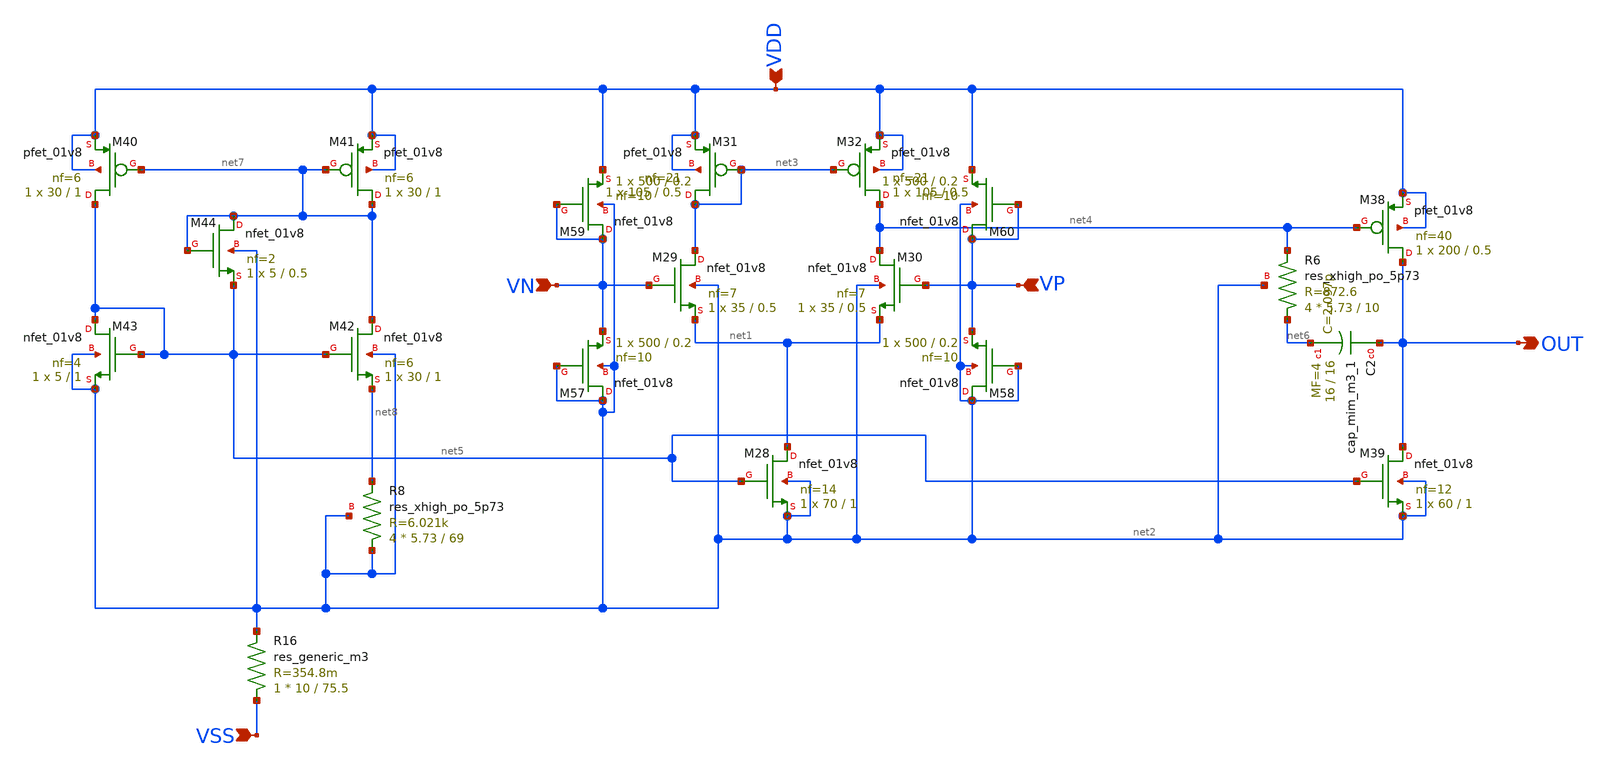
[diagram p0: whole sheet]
** sch_path: DeltaSigma/xschem/C2S2_Amp_F_I.sch
**.subckt C2S2_Amp_F_I VN VDD VSS VP OUT
*.ipin VN
*.ipin VDD
*.ipin VSS
*.ipin VP
*.opin OUT
XM28 net1 net5 net2 net2 sky130_fd_pr__nfet_01v8 L=1 W=70 nf=14 ad='int((nf+1)/2) * W/nf * 0.29' as='int((nf+2)/2) * W/nf * 0.29'
+ pd='2*int((nf+1)/2) * (W/nf + 0.29)' ps='2*int((nf+2)/2) * (W/nf + 0.29)' nrd='0.29 / W' nrs='0.29 / W'
+ sa=0 sb=0 sd=0 mult=1 m=1
XM29 net3 VN net1 net2 sky130_fd_pr__nfet_01v8 L=0.5 W=35 nf=7 ad='int((nf+1)/2) * W/nf * 0.29' as='int((nf+2)/2) * W/nf * 0.29'
+ pd='2*int((nf+1)/2) * (W/nf + 0.29)' ps='2*int((nf+2)/2) * (W/nf + 0.29)' nrd='0.29 / W' nrs='0.29 / W'
+ sa=0 sb=0 sd=0 mult=1 m=1
XM30 net4 VP net1 net2 sky130_fd_pr__nfet_01v8 L=0.5 W=35 nf=7 ad='int((nf+1)/2) * W/nf * 0.29' as='int((nf+2)/2) * W/nf * 0.29'
+ pd='2*int((nf+1)/2) * (W/nf + 0.29)' ps='2*int((nf+2)/2) * (W/nf + 0.29)' nrd='0.29 / W' nrs='0.29 / W'
+ sa=0 sb=0 sd=0 mult=1 m=1
XM31 net3 net3 VDD VDD sky130_fd_pr__pfet_01v8 L=0.5 W=105 nf=21 ad='int((nf+1)/2) * W/nf * 0.29' as='int((nf+2)/2) * W/nf * 0.29'
+ pd='2*int((nf+1)/2) * (W/nf + 0.29)' ps='2*int((nf+2)/2) * (W/nf + 0.29)' nrd='0.29 / W' nrs='0.29 / W'
+ sa=0 sb=0 sd=0 mult=1 m=1
XM32 net4 net3 VDD VDD sky130_fd_pr__pfet_01v8 L=0.5 W=105 nf=21 ad='int((nf+1)/2) * W/nf * 0.29' as='int((nf+2)/2) * W/nf * 0.29'
+ pd='2*int((nf+1)/2) * (W/nf + 0.29)' ps='2*int((nf+2)/2) * (W/nf + 0.29)' nrd='0.29 / W' nrs='0.29 / W'
+ sa=0 sb=0 sd=0 mult=1 m=1
XM38 OUT net4 VDD VDD sky130_fd_pr__pfet_01v8 L=0.5 W=200 nf=40 ad='int((nf+1)/2) * W/nf * 0.29' as='int((nf+2)/2) * W/nf * 0.29'
+ pd='2*int((nf+1)/2) * (W/nf + 0.29)' ps='2*int((nf+2)/2) * (W/nf + 0.29)' nrd='0.29 / W' nrs='0.29 / W'
+ sa=0 sb=0 sd=0 mult=1 m=1
XM39 OUT net5 net2 net2 sky130_fd_pr__nfet_01v8 L=1 W=60 nf=12 ad='int((nf+1)/2) * W/nf * 0.29' as='int((nf+2)/2) * W/nf * 0.29'
+ pd='2*int((nf+1)/2) * (W/nf + 0.29)' ps='2*int((nf+2)/2) * (W/nf + 0.29)' nrd='0.29 / W' nrs='0.29 / W'
+ sa=0 sb=0 sd=0 mult=1 m=1
XC2 OUT net6 sky130_fd_pr__cap_mim_m3_1 W=16 L=16 MF=4 m=4
XR6 net6 net4 net2 sky130_fd_pr__res_xhigh_po_5p73 L=10 mult=4 m=4
XM40 net5 net7 VDD VDD sky130_fd_pr__pfet_01v8 L=1 W=30 nf=6 ad='int((nf+1)/2) * W/nf * 0.29' as='int((nf+2)/2) * W/nf * 0.29'
+ pd='2*int((nf+1)/2) * (W/nf + 0.29)' ps='2*int((nf+2)/2) * (W/nf + 0.29)' nrd='0.29 / W' nrs='0.29 / W'
+ sa=0 sb=0 sd=0 mult=1 m=1
XM41 net7 net7 VDD VDD sky130_fd_pr__pfet_01v8 L=1 W=30 nf=6 ad='int((nf+1)/2) * W/nf * 0.29' as='int((nf+2)/2) * W/nf * 0.29'
+ pd='2*int((nf+1)/2) * (W/nf + 0.29)' ps='2*int((nf+2)/2) * (W/nf + 0.29)' nrd='0.29 / W' nrs='0.29 / W'
+ sa=0 sb=0 sd=0 mult=1 m=1
XM42 net7 net5 net8 net2 sky130_fd_pr__nfet_01v8 L=1 W=30 nf=6 ad='int((nf+1)/2) * W/nf * 0.29' as='int((nf+2)/2) * W/nf * 0.29'
+ pd='2*int((nf+1)/2) * (W/nf + 0.29)' ps='2*int((nf+2)/2) * (W/nf + 0.29)' nrd='0.29 / W' nrs='0.29 / W'
+ sa=0 sb=0 sd=0 mult=1 m=1
XM43 net5 net5 net2 net2 sky130_fd_pr__nfet_01v8 L=1 W=5 nf=4 ad='int((nf+1)/2) * W/nf * 0.29' as='int((nf+2)/2) * W/nf * 0.29'
+ pd='2*int((nf+1)/2) * (W/nf + 0.29)' ps='2*int((nf+2)/2) * (W/nf + 0.29)' nrd='0.29 / W' nrs='0.29 / W'
+ sa=0 sb=0 sd=0 mult=1 m=1
XM44 net7 net7 net5 net2 sky130_fd_pr__nfet_01v8 L=0.5 W=5 nf=2 ad='int((nf+1)/2) * W/nf * 0.29' as='int((nf+2)/2) * W/nf * 0.29'
+ pd='2*int((nf+1)/2) * (W/nf + 0.29)' ps='2*int((nf+2)/2) * (W/nf + 0.29)' nrd='0.29 / W' nrs='0.29 / W'
+ sa=0 sb=0 sd=0 mult=1 m=1
XR8 net2 net8 net2 sky130_fd_pr__res_xhigh_po_5p73 L=69 mult=4 m=4
R16 VSS net2 sky130_fd_pr__res_generic_m3 W=10 L=75.5 m=1
XM57 net2 net2 VN net2 sky130_fd_pr__nfet_01v8 L=0.2 W=500 nf=10 ad='int((nf+1)/2) * W/nf * 0.29' as='int((nf+2)/2) * W/nf * 0.29'
+ pd='2*int((nf+1)/2) * (W/nf + 0.29)' ps='2*int((nf+2)/2) * (W/nf + 0.29)' nrd='0.29 / W' nrs='0.29 / W'
+ sa=0 sb=0 sd=0 mult=1 m=1
XM58 net2 net2 VP net2 sky130_fd_pr__nfet_01v8 L=0.2 W=500 nf=10 ad='int((nf+1)/2) * W/nf * 0.29' as='int((nf+2)/2) * W/nf * 0.29'
+ pd='2*int((nf+1)/2) * (W/nf + 0.29)' ps='2*int((nf+2)/2) * (W/nf + 0.29)' nrd='0.29 / W' nrs='0.29 / W'
+ sa=0 sb=0 sd=0 mult=1 m=1
XM59 VN VN VDD net2 sky130_fd_pr__nfet_01v8 L=0.2 W=500 nf=10 ad='int((nf+1)/2) * W/nf * 0.29' as='int((nf+2)/2) * W/nf * 0.29'
+ pd='2*int((nf+1)/2) * (W/nf + 0.29)' ps='2*int((nf+2)/2) * (W/nf + 0.29)' nrd='0.29 / W' nrs='0.29 / W'
+ sa=0 sb=0 sd=0 mult=1 m=1
XM60 VP VP VDD net2 sky130_fd_pr__nfet_01v8 L=0.2 W=500 nf=10 ad='int((nf+1)/2) * W/nf * 0.29' as='int((nf+2)/2) * W/nf * 0.29'
+ pd='2*int((nf+1)/2) * (W/nf + 0.29)' ps='2*int((nf+2)/2) * (W/nf + 0.29)' nrd='0.29 / W' nrs='0.29 / W'
+ sa=0 sb=0 sd=0 mult=1 m=1
**.ends
.end
